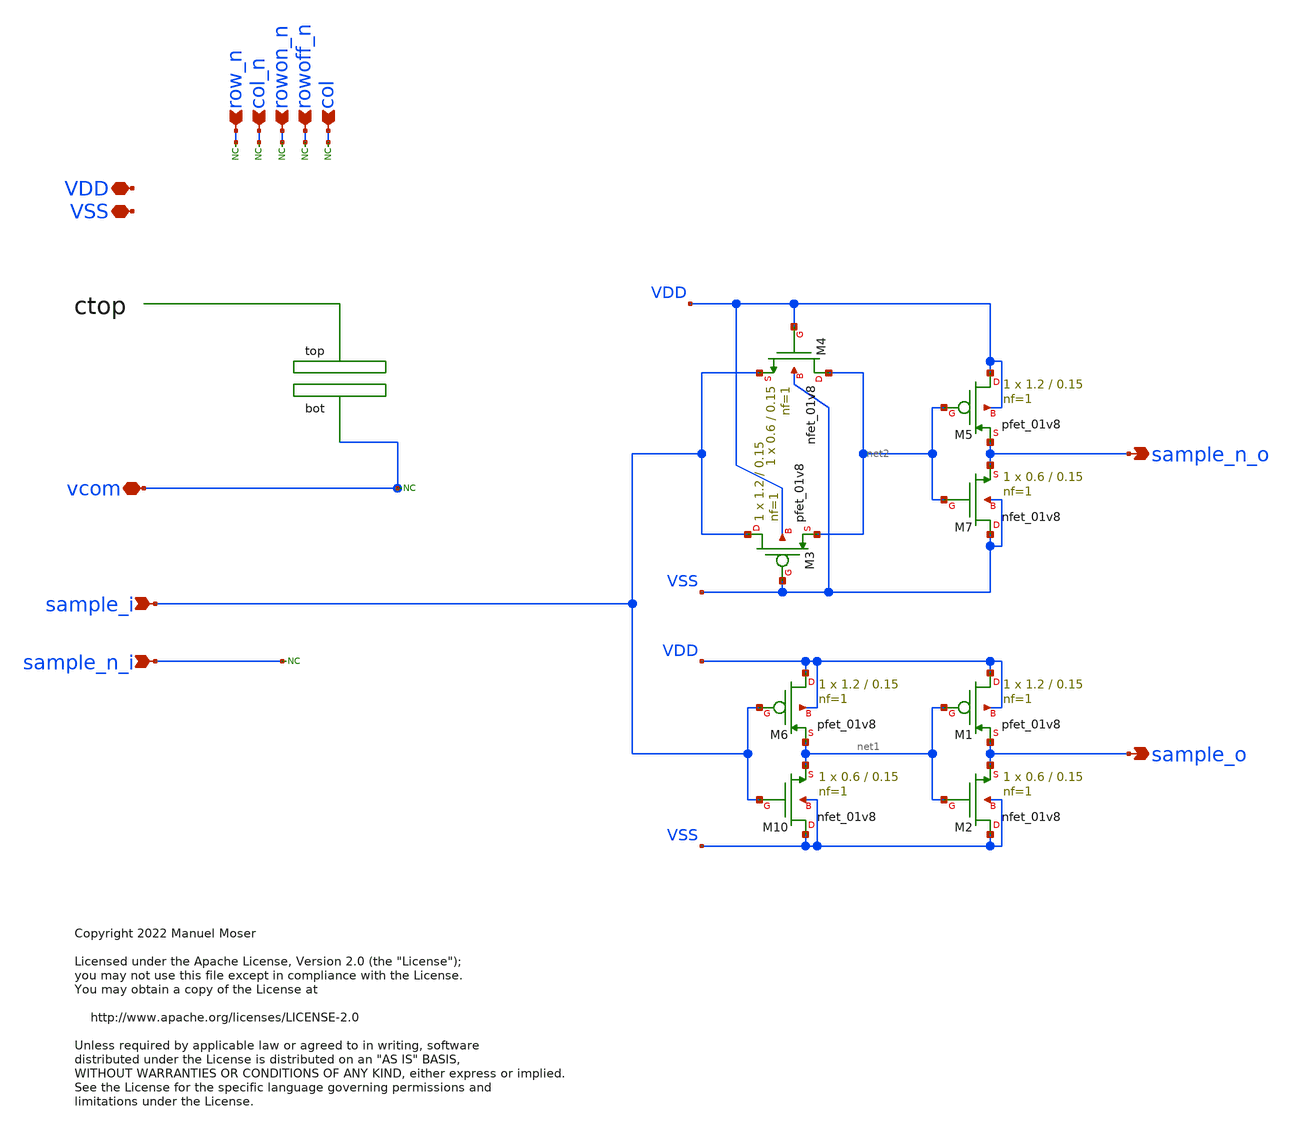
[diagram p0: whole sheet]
** sch_path: xschem/adc_array_circuit_drv.sch
* Copyright 2022 Manuel Moser
* Licensed under the Apache License, Version 2.0 (the "License");
**.subckt adc_array_circuit_drv sample_n_i sample_i vcom row_n col_n rowon_n VDD VSS sample_o
*+ sample_n_o rowoff_n col
*.ipin sample_n_i
*.ipin sample_i
*.iopin vcom
*.ipin row_n
*.ipin col_n
*.ipin rowon_n
*.iopin VDD
*.iopin VSS
*.opin sample_o
*.opin sample_n_o
*.ipin rowoff_n
*.ipin col
XM6 VDD sample_i net1 VDD sky130_fd_pr__pfet_01v8 L=0.15 W=1.2 nf=1 ad='int((nf+1)/2) * W/nf * 0.29'
+ as='int((nf+2)/2) * W/nf * 0.29' pd='2*int((nf+1)/2) * (W/nf + 0.29)' ps='2*int((nf+2)/2) * (W/nf + 0.29)'
+ nrd='0.29 / W' nrs='0.29 / W' sa=0 sb=0 sd=0 mult=1 m=1
XM10 VSS sample_i net1 VSS sky130_fd_pr__nfet_01v8 L=0.15 W=0.6 nf=1 ad='int((nf+1)/2) * W/nf * 0.29'
+ as='int((nf+2)/2) * W/nf * 0.29' pd='2*int((nf+1)/2) * (W/nf + 0.29)' ps='2*int((nf+2)/2) * (W/nf + 0.29)'
+ nrd='0.29 / W' nrs='0.29 / W' sa=0 sb=0 sd=0 mult=1 m=1
* noconn row_n
* noconn col_n
* noconn rowon_n
* noconn vcom
* noconn rowoff_n
* noconn col
XM1 VDD net1 sample_o VDD sky130_fd_pr__pfet_01v8 L=0.15 W=1.2 nf=1 ad='int((nf+1)/2) * W/nf * 0.29'
+ as='int((nf+2)/2) * W/nf * 0.29' pd='2*int((nf+1)/2) * (W/nf + 0.29)' ps='2*int((nf+2)/2) * (W/nf + 0.29)'
+ nrd='0.29 / W' nrs='0.29 / W' sa=0 sb=0 sd=0 mult=1 m=1
XM2 VSS net1 sample_o VSS sky130_fd_pr__nfet_01v8 L=0.15 W=0.6 nf=1 ad='int((nf+1)/2) * W/nf * 0.29'
+ as='int((nf+2)/2) * W/nf * 0.29' pd='2*int((nf+1)/2) * (W/nf + 0.29)' ps='2*int((nf+2)/2) * (W/nf + 0.29)'
+ nrd='0.29 / W' nrs='0.29 / W' sa=0 sb=0 sd=0 mult=1 m=1
* noconn sample_n_i
XM3 sample_i VSS net2 VDD sky130_fd_pr__pfet_01v8 L=0.15 W=1.2 nf=1 ad='int((nf+1)/2) * W/nf * 0.29'
+ as='int((nf+2)/2) * W/nf * 0.29' pd='2*int((nf+1)/2) * (W/nf + 0.29)' ps='2*int((nf+2)/2) * (W/nf + 0.29)'
+ nrd='0.29 / W' nrs='0.29 / W' sa=0 sb=0 sd=0 mult=1 m=1
XM4 net2 VDD sample_i VSS sky130_fd_pr__nfet_01v8 L=0.15 W=0.6 nf=1 ad='int((nf+1)/2) * W/nf * 0.29'
+ as='int((nf+2)/2) * W/nf * 0.29' pd='2*int((nf+1)/2) * (W/nf + 0.29)' ps='2*int((nf+2)/2) * (W/nf + 0.29)'
+ nrd='0.29 / W' nrs='0.29 / W' sa=0 sb=0 sd=0 mult=1 m=1
XM5 VDD net2 sample_n_o VDD sky130_fd_pr__pfet_01v8 L=0.15 W=1.2 nf=1 ad='int((nf+1)/2) * W/nf * 0.29'
+ as='int((nf+2)/2) * W/nf * 0.29' pd='2*int((nf+1)/2) * (W/nf + 0.29)' ps='2*int((nf+2)/2) * (W/nf + 0.29)'
+ nrd='0.29 / W' nrs='0.29 / W' sa=0 sb=0 sd=0 mult=1 m=1
XM7 VSS net2 sample_n_o VSS sky130_fd_pr__nfet_01v8 L=0.15 W=0.6 nf=1 ad='int((nf+1)/2) * W/nf * 0.29'
+ as='int((nf+2)/2) * W/nf * 0.29' pd='2*int((nf+1)/2) * (W/nf + 0.29)' ps='2*int((nf+2)/2) * (W/nf + 0.29)'
+ nrd='0.29 / W' nrs='0.29 / W' sa=0 sb=0 sd=0 mult=1 m=1
**.ends
.end
